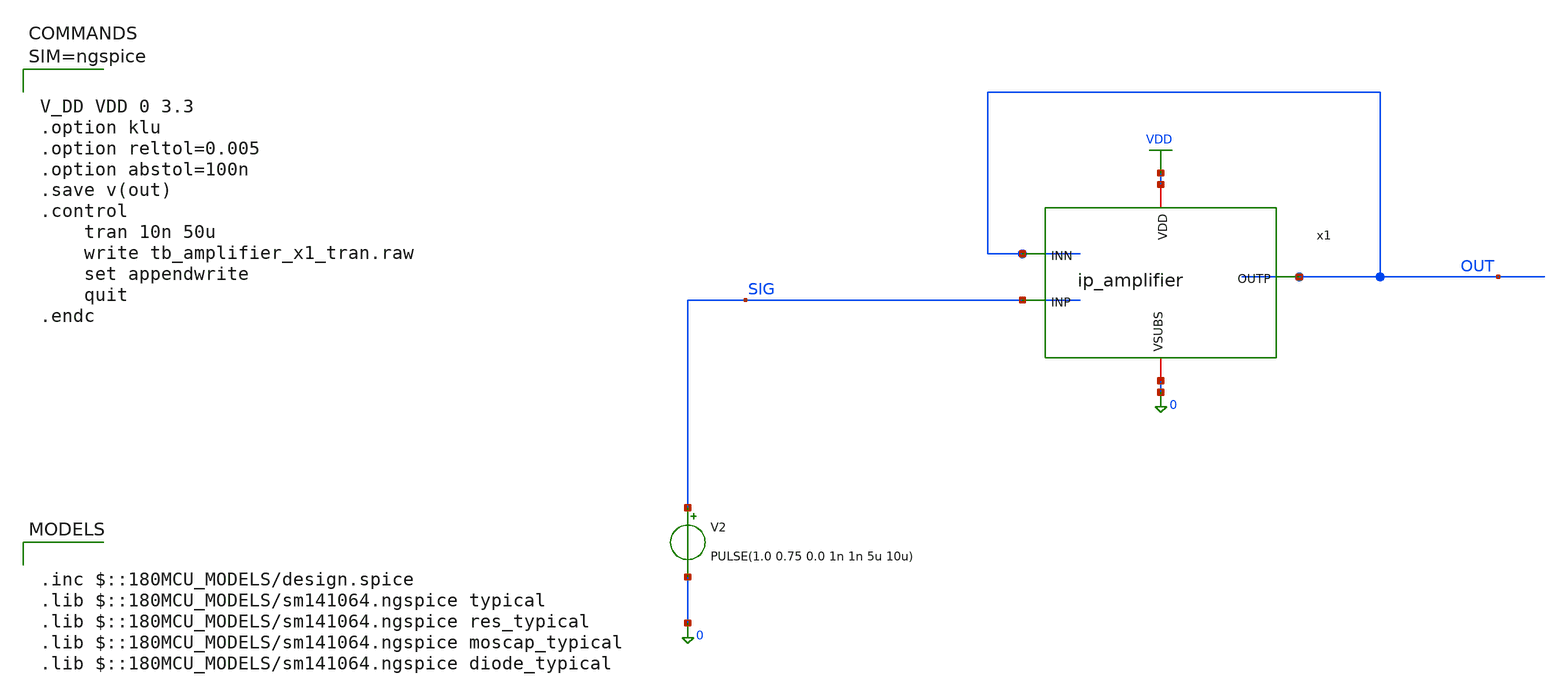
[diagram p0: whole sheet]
** sch_path: xschem/tb_amplifier_x1_tran.sch
**.subckt tb_amplifier_x1_tran
V2 SIG 0 PULSE(1.0 0.75 0.0 1n 1n 5u 10u)
x1 VDD OUT SIG OUT 0 ip_amplifier
**** begin user architecture code

.inc $::180MCU_MODELS/design.spice
.lib $::180MCU_MODELS/sm141064.ngspice typical
.lib $::180MCU_MODELS/sm141064.ngspice res_typical
.lib $::180MCU_MODELS/sm141064.ngspice moscap_typical
.lib $::180MCU_MODELS/sm141064.ngspice diode_typical




V_DD VDD 0 3.3
.option klu
.option reltol=0.005
.option abstol=100n
.save v(out)
.control
	tran 10n 50u
	write tb_amplifier_x1_tran.raw
	set appendwrite
	quit
.endc



**** end user architecture code
**.ends
.GLOBAL VDD
.end
